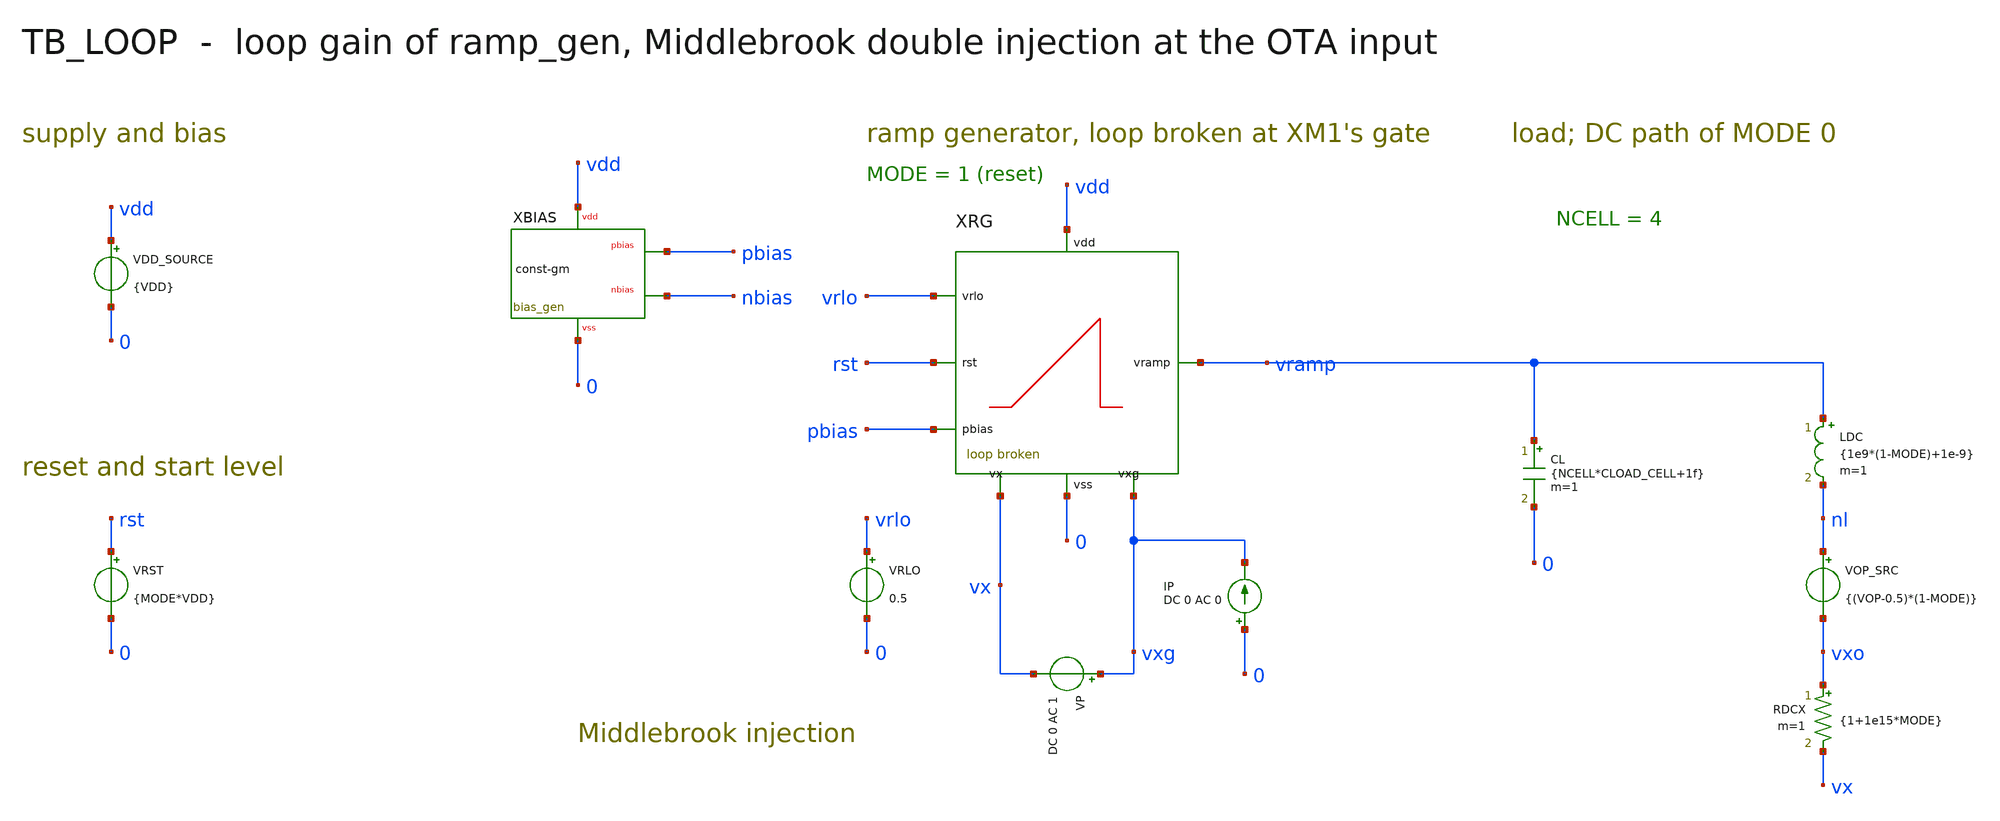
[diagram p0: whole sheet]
** sch_path: mixed_signal/ramp_gen/tb_loop.sch
**.subckt tb_loop
VDD_SOURCE vdd 0 {VDD}
XBIAS vdd 0 pbias nbias bias_gen
VRST rst 0 {MODE*VDD}
VRLO vrlo 0 0.5
XRG vramp rst vrlo pbias vdd 0 vx vxg ramp_gen_lb
VP vxg vx DC 0 AC 1
IP 0 vxg DC 0 AC 0
CL vramp 0 {NCELL*CLOAD_CELL+1f} m=1
LDC vramp nl {1e9*(1-MODE)+1e-9} m=1
VOP_SRC nl vxo {(VOP-0.5)*(1-MODE)}
RDCX vxo vx {1+1e15*MODE} m=1
**** begin user architecture code

.include /foss/pdks/gf180mcuD/libs.tech/ngspice/design.ngspice
.lib /foss/pdks/gf180mcuD/libs.tech/ngspice/sm141064.ngspice typical
.lib /foss/pdks/gf180mcuD/libs.tech/ngspice/sm141064.ngspice res_typical
.lib /foss/pdks/gf180mcuD/libs.tech/ngspice/sm141064.ngspice mimcap_typical
.lib /foss/pdks/gf180mcuD/libs.tech/ngspice/sm141064.ngspice moscap_typical
.include /foss/designs/mixed_signal/ramp_gen/ref/bias_gen/data/bias_gen_params.spice
.include /foss/designs/mixed_signal/ramp_gen/ref/bias_gen/bias_gen.spice
.include /foss/designs/mixed_signal/ramp_gen/data/ramp_gen_params.spice
.include /foss/designs/mixed_signal/ramp_gen/work/ramp_gen_lb.spice
.param VDD=3.3
.param CLOAD_CELL=10f
.param MODE=1
.param VOP=0.5
.param NCELL=4
.options gmin=1e-15
.control
set num_threads=1
set wr_singlescale
set wr_vecnames
op
let op_vramp = v(vramp)
let op_vx = v(vx)
print op_vramp op_vx
ac dec 40 1k 1G
let tv = -v(vx)/v(vxg)
setplot const
alter VP acmag=0
alter IP acmag=1
ac dec 40 1k 1G
let ipr = i(vp)
let ti = -ipr/(1-ipr)
let tv = ac1.tv
let t = (tv*ti-1)/(tv+ti+2)
let tmag = db(t)
let tph = 180/pi*cph(t)
wrdata loop.csv tmag tph
quit
.endc

**** end user architecture code
**.ends
.end
